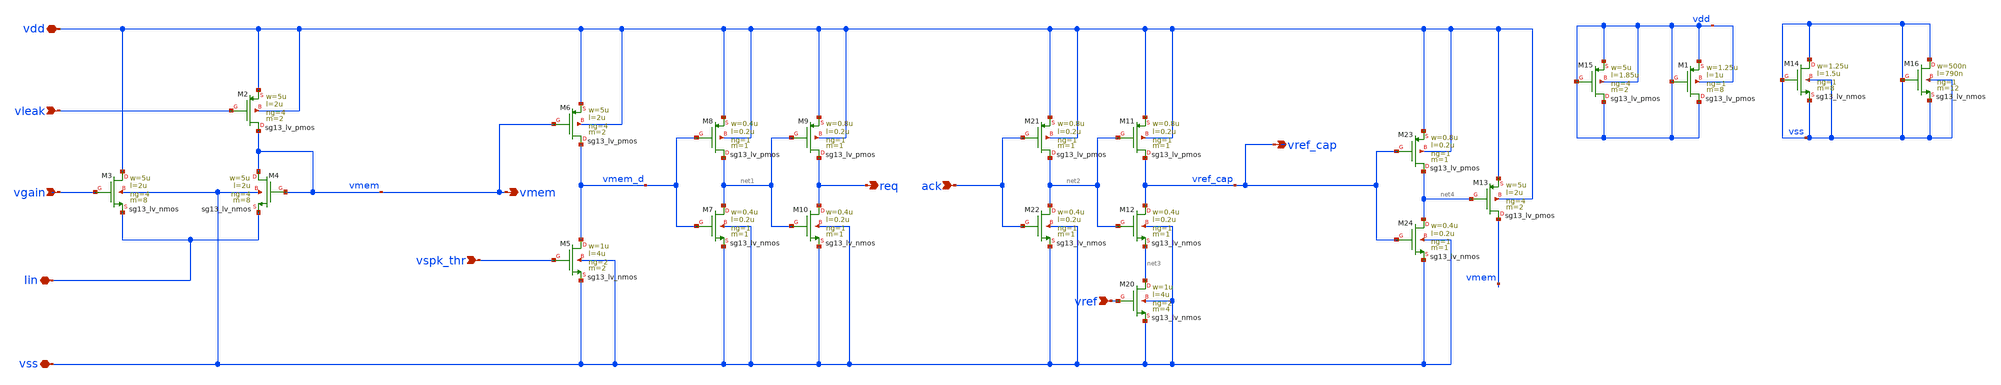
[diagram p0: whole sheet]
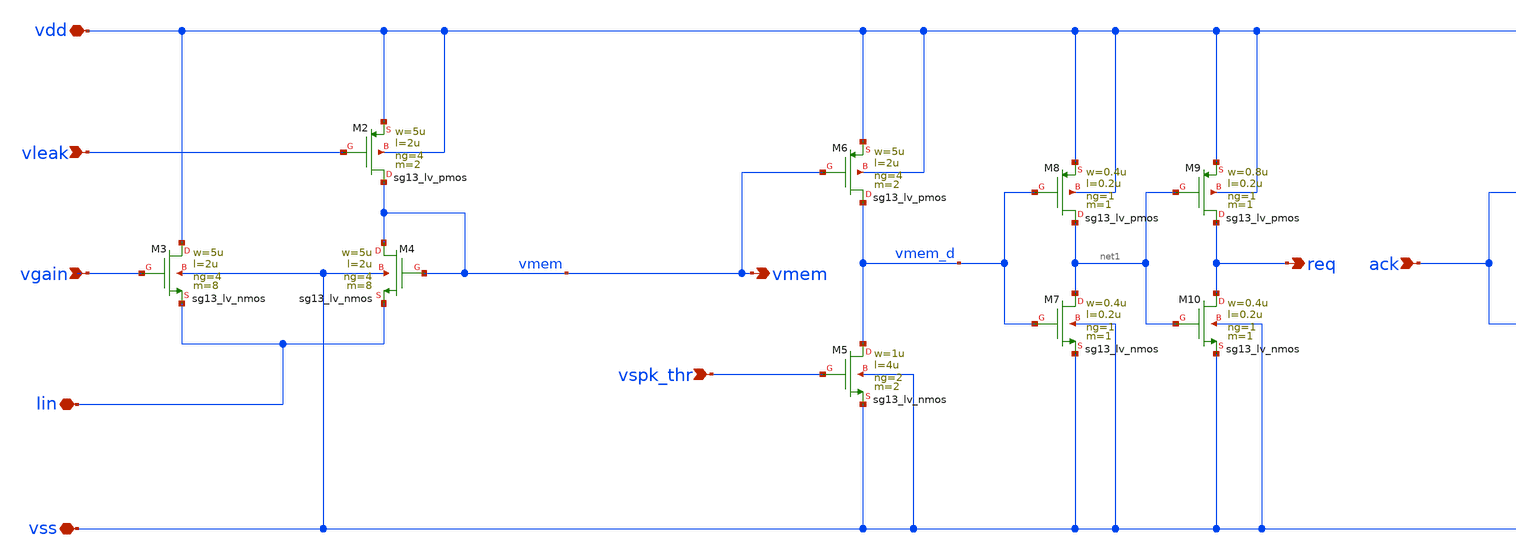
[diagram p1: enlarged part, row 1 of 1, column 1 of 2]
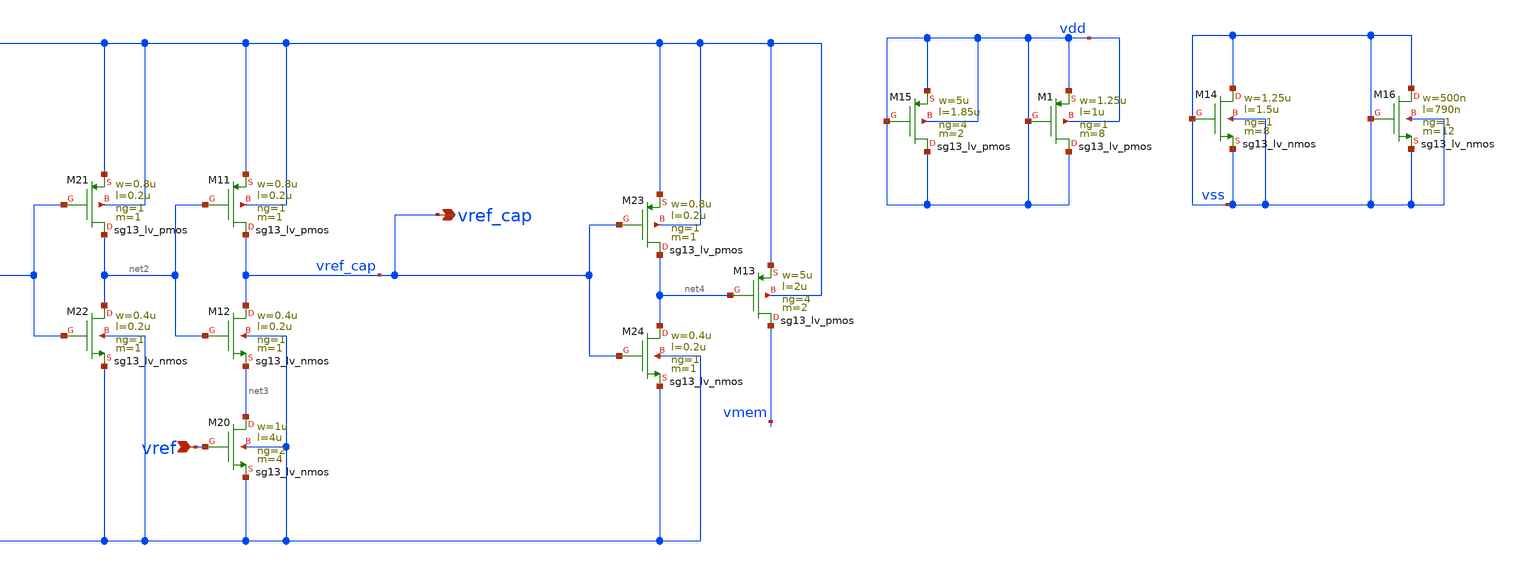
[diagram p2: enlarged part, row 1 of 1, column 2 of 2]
** sch_path: v2_feature_extr_withf/neuron_n_ADC_nocap.sch
**.subckt neuron_n_ADC_nocap vdd vss Iin vleak vspk_thr vref ack vmem req vgain vref_cap
*.iopin vdd
*.iopin vss
*.iopin Iin
*.ipin vleak
*.ipin vspk_thr
*.ipin vref
*.ipin ack
*.opin vmem
*.opin req
*.ipin vgain
*.opin vref_cap
XM2 vmem vleak vdd vdd sg13_lv_pmos w=5u l=2u ng=4 m=2 mm_ok=1
XM3 vdd vgain Iin vss sg13_lv_nmos w=5u l=2u ng=4 m=8 mm_ok=1
XM4 vmem vmem Iin vss sg13_lv_nmos w=5u l=2u ng=4 m=8 mm_ok=1
XM5 vmem_d vspk_thr vss vss sg13_lv_nmos w=1u l=4u ng=2 m=2 mm_ok=1
XM6 vmem_d vmem vdd vdd sg13_lv_pmos w=5u l=2u ng=4 m=2 mm_ok=1
XM7 net1 vmem_d vss vss sg13_lv_nmos w=0.4u l=0.2u ng=1 m=1 mm_ok=1
XM8 net1 vmem_d vdd vdd sg13_lv_pmos w=0.4u l=0.2u ng=1 m=1 mm_ok=1
XM9 req net1 vdd vdd sg13_lv_pmos w=0.8u l=0.2u ng=1 m=1 mm_ok=1
XM10 req net1 vss vss sg13_lv_nmos w=0.4u l=0.2u ng=1 m=1 mm_ok=1
XM11 vref_cap net2 vdd vdd sg13_lv_pmos w=0.8u l=0.2u ng=1 m=1 mm_ok=1
XM12 vref_cap net2 net3 vss sg13_lv_nmos w=0.4u l=0.2u ng=1 m=1 mm_ok=1
XM13 vmem net4 vdd vdd sg13_lv_pmos w=5u l=2u ng=4 m=2 mm_ok=1
XM20 net3 vref vss vss sg13_lv_nmos w=1u l=4u ng=2 m=4 mm_ok=1
XM21 net2 ack vdd vdd sg13_lv_pmos w=0.8u l=0.2u ng=1 m=1 mm_ok=1
XM22 net2 ack vss vss sg13_lv_nmos w=0.4u l=0.2u ng=1 m=1 mm_ok=1
XM23 net4 vref_cap vdd vdd sg13_lv_pmos w=0.8u l=0.2u ng=1 m=1 mm_ok=1
XM24 net4 vref_cap vss vss sg13_lv_nmos w=0.4u l=0.2u ng=1 m=1 mm_ok=1
XM1 vdd vdd vdd vdd sg13_lv_pmos w=1.25u l=1u ng=1 m=8 mm_ok=1
XM14 vss vss vss vss sg13_lv_nmos w=1.25u l=1.5u ng=1 m=8 mm_ok=1
XM16 vss vss vss vss sg13_lv_nmos w=500n l=790n ng=1 m=12 mm_ok=1
XM15 vdd vdd vdd vdd sg13_lv_pmos w=5u l=1.85u ng=4 m=2 mm_ok=1
**.ends
.end
